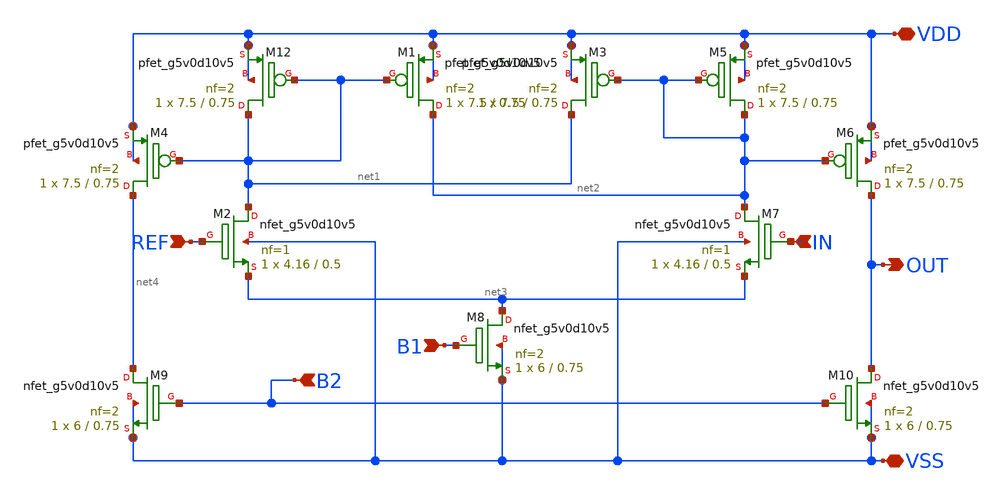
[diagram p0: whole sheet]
** sch_path: komparator_5v_fix/komparator_5/komparator.sch
**.subckt komparator VDD VSS OUT IN REF B1 B2
*.iopin VDD
*.iopin VSS
*.opin OUT
*.ipin IN
*.ipin REF
*.ipin B1
*.ipin B2
XM12 net1 net1 VDD VDD sky130_fd_pr__pfet_g5v0d10v5 L=0.75 W=7.5 nf=2 ad='int((2 + 1)/2) * 7.5 / 2 * 0.29'
+ as='int((2 + 2)/2) * 7.5 / 2 * 0.29' pd='2*int((2 + 1)/2) * (7.5 / 2 + 0.29)' ps='2*int((2 + 2)/2) * (7.5 / 2 + 0.29)'
+ nrd='0.29 / 7.5 ' nrs='0.29 / 7.5 ' sa=0 sb=0 sd=0 mult=1 m=1
XM1 net2 net1 VDD VDD sky130_fd_pr__pfet_g5v0d10v5 L=0.75 W=7.5 nf=2 ad='int((2 + 1)/2) * 7.5 / 2 * 0.29'
+ as='int((2 + 2)/2) * 7.5 / 2 * 0.29' pd='2*int((2 + 1)/2) * (7.5 / 2 + 0.29)' ps='2*int((2 + 2)/2) * (7.5 / 2 + 0.29)'
+ nrd='0.29 / 7.5 ' nrs='0.29 / 7.5 ' sa=0 sb=0 sd=0 mult=1 m=1
XM3 net1 net2 VDD VDD sky130_fd_pr__pfet_g5v0d10v5 L=0.75 W=7.5 nf=2 ad='int((2 + 1)/2) * 7.5 / 2 * 0.29'
+ as='int((2 + 2)/2) * 7.5 / 2 * 0.29' pd='2*int((2 + 1)/2) * (7.5 / 2 + 0.29)' ps='2*int((2 + 2)/2) * (7.5 / 2 + 0.29)'
+ nrd='0.29 / 7.5 ' nrs='0.29 / 7.5 ' sa=0 sb=0 sd=0 mult=1 m=1
XM5 net2 net2 VDD VDD sky130_fd_pr__pfet_g5v0d10v5 L=0.75 W=7.5 nf=2 ad='int((2 + 1)/2) * 7.5 / 2 * 0.29'
+ as='int((2 + 2)/2) * 7.5 / 2 * 0.29' pd='2*int((2 + 1)/2) * (7.5 / 2 + 0.29)' ps='2*int((2 + 2)/2) * (7.5 / 2 + 0.29)'
+ nrd='0.29 / 7.5 ' nrs='0.29 / 7.5 ' sa=0 sb=0 sd=0 mult=1 m=1
XM6 OUT net2 VDD VDD sky130_fd_pr__pfet_g5v0d10v5 L=0.75 W=7.5 nf=2 ad='int((2 + 1)/2) * 7.5 / 2 * 0.29'
+ as='int((2 + 2)/2) * 7.5 / 2 * 0.29' pd='2*int((2 + 1)/2) * (7.5 / 2 + 0.29)' ps='2*int((2 + 2)/2) * (7.5 / 2 + 0.29)'
+ nrd='0.29 / 7.5 ' nrs='0.29 / 7.5 ' sa=0 sb=0 sd=0 mult=1 m=1
XM2 net1 REF net3 VSS sky130_fd_pr__nfet_g5v0d10v5 L=0.5 W=4.16 nf=1 ad='int((1 + 1)/2) * 4.16 / 1 * 0.29'
+ as='int((1 + 2)/2) * 4.16 / 1 * 0.29' pd='2*int((1 + 1)/2) * (4.16 / 1 + 0.29)' ps='2*int((1 + 2)/2) * (4.16 / 1 + 0.29)'
+ nrd='0.29 / 4.16 ' nrs='0.29 / 4.16 ' sa=0 sb=0 sd=0 mult=1 m=1
XM7 net2 IN net3 VSS sky130_fd_pr__nfet_g5v0d10v5 L=0.5 W=4.16 nf=1 ad='int((1 + 1)/2) * 4.16 / 1 * 0.29'
+ as='int((1 + 2)/2) * 4.16 / 1 * 0.29' pd='2*int((1 + 1)/2) * (4.16 / 1 + 0.29)' ps='2*int((1 + 2)/2) * (4.16 / 1 + 0.29)'
+ nrd='0.29 / 4.16 ' nrs='0.29 / 4.16 ' sa=0 sb=0 sd=0 mult=1 m=1
XM8 net3 B1 VSS VSS sky130_fd_pr__nfet_g5v0d10v5 L=0.75 W=6 nf=2 ad='int((2 + 1)/2) * 6 / 2 * 0.29' as='int((2 + 2)/2) * 6 / 2 * 0.29'
+ pd='2*int((2 + 1)/2) * (6 / 2 + 0.29)' ps='2*int((2 + 2)/2) * (6 / 2 + 0.29)' nrd='0.29 / 6 ' nrs='0.29 / 6 '
+ sa=0 sb=0 sd=0 mult=1 m=1
XM9 net4 B2 VSS VSS sky130_fd_pr__nfet_g5v0d10v5 L=0.75 W=6 nf=2 ad='int((2 + 1)/2) * 6 / 2 * 0.29' as='int((2 + 2)/2) * 6 / 2 * 0.29'
+ pd='2*int((2 + 1)/2) * (6 / 2 + 0.29)' ps='2*int((2 + 2)/2) * (6 / 2 + 0.29)' nrd='0.29 / 6 ' nrs='0.29 / 6 '
+ sa=0 sb=0 sd=0 mult=1 m=1
XM10 OUT B2 VSS VSS sky130_fd_pr__nfet_g5v0d10v5 L=0.75 W=6 nf=2 ad='int((2 + 1)/2) * 6 / 2 * 0.29' as='int((2 + 2)/2) * 6 / 2 * 0.29'
+ pd='2*int((2 + 1)/2) * (6 / 2 + 0.29)' ps='2*int((2 + 2)/2) * (6 / 2 + 0.29)' nrd='0.29 / 6 ' nrs='0.29 / 6 '
+ sa=0 sb=0 sd=0 mult=1 m=1
XM4 net4 net1 VDD VDD sky130_fd_pr__pfet_g5v0d10v5 L=0.75 W=7.5 nf=2 ad='int((2 + 1)/2) * 7.5 / 2 * 0.29'
+ as='int((2 + 2)/2) * 7.5 / 2 * 0.29' pd='2*int((2 + 1)/2) * (7.5 / 2 + 0.29)' ps='2*int((2 + 2)/2) * (7.5 / 2 + 0.29)'
+ nrd='0.29 / 7.5 ' nrs='0.29 / 7.5 ' sa=0 sb=0 sd=0 mult=1 m=1
**.ends
.end
